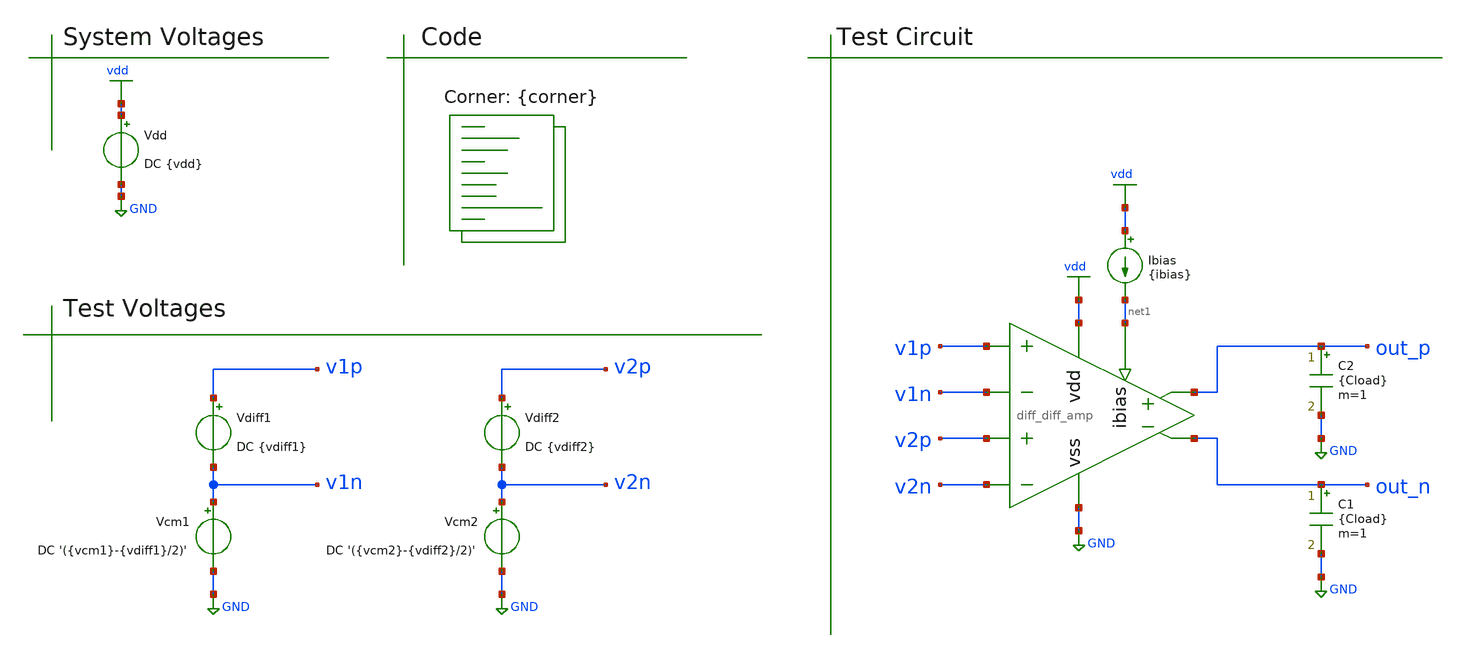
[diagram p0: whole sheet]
** sch_path: tb/tb_diffdiff_transfer.sch
**.subckt tb_diffdiff_transfer
Vdd vdd GND DC {vdd}
C1 out_n GND {Cload} m=1
Vdiff1 v1p v1n DC {vdiff1}
Vcm1 v1n GND DC '({vcm1}-{vdiff1}/2)'
C2 out_p GND {Cload} m=1
Vdiff2 v2p v2n DC {vdiff2}
Vcm2 v2n GND DC '({vcm2}-{vdiff2}/2)'
Ibias vdd net1 {ibias}
x1 v1p v1n v2p v2n out_p out_n net1 vdd GND diff_diff_amp
**** begin user architecture code


.option TEMP={temperature}
.option warn=1
.control
save out_p, out_n, i(vdd)
dc Vdiff1 -0.9 0.9 0.05
wrdata {output_file} V(out_p) V(out_n) I(vdd)
quit
.endc


.lib $::SKYWATER_MODELS/sky130.lib.spice {corner}
**** end user architecture code
**.ends

* expanding   symbol:  /home/moduhub/work/sky130_ak_ip__sigma_delta/sch/diff_diff_amp.sym # of
*+ pins=9
** sym_path: sch/diff_diff_amp.sym
** sch_path: sch/diff_diff_amp.sch
.subckt diff_diff_amp v1p v1n v2p v2n vo_p vo_n ibias vdd vss
*.ipin v1p
*.ipin v1n
*.ipin v2p
*.ipin v2n
*.ipin vss
*.ipin vdd
*.ipin ibias
*.opin vo_n
*.opin vo_p
XM1 net1 ibias vss vss sky130_fd_pr__nfet_01v8 L=0.5 W=10 nf=1 ad='int((nf+1)/2) * W/nf * 0.29' as='int((nf+2)/2) * W/nf * 0.29'
+ pd='2*int((nf+1)/2) * (W/nf + 0.29)' ps='2*int((nf+2)/2) * (W/nf + 0.29)' nrd='0.29 / W' nrs='0.29 / W'
+ sa=0 sb=0 sd=0 mult=1 m=1
XM2 net2 ibias vss vss sky130_fd_pr__nfet_01v8 L=0.5 W=10 nf=1 ad='int((nf+1)/2) * W/nf * 0.29' as='int((nf+2)/2) * W/nf * 0.29'
+ pd='2*int((nf+1)/2) * (W/nf + 0.29)' ps='2*int((nf+2)/2) * (W/nf + 0.29)' nrd='0.29 / W' nrs='0.29 / W'
+ sa=0 sb=0 sd=0 mult=1 m=1
XM3 ibias ibias vss vss sky130_fd_pr__nfet_01v8 L=0.5 W=1 nf=1 ad='int((nf+1)/2) * W/nf * 0.29' as='int((nf+2)/2) * W/nf * 0.29'
+ pd='2*int((nf+1)/2) * (W/nf + 0.29)' ps='2*int((nf+2)/2) * (W/nf + 0.29)' nrd='0.29 / W' nrs='0.29 / W'
+ sa=0 sb=0 sd=0 mult=1 m=1
XM4 vo_n v1p net1 vss sky130_fd_pr__nfet_01v8 L=1 W=4 nf=1 ad='int((nf+1)/2) * W/nf * 0.29' as='int((nf+2)/2) * W/nf * 0.29'
+ pd='2*int((nf+1)/2) * (W/nf + 0.29)' ps='2*int((nf+2)/2) * (W/nf + 0.29)' nrd='0.29 / W' nrs='0.29 / W'
+ sa=0 sb=0 sd=0 mult=1 m=1
XM5 vo_p v1n net1 vss sky130_fd_pr__nfet_01v8 L=1 W=4 nf=1 ad='int((nf+1)/2) * W/nf * 0.29' as='int((nf+2)/2) * W/nf * 0.29'
+ pd='2*int((nf+1)/2) * (W/nf + 0.29)' ps='2*int((nf+2)/2) * (W/nf + 0.29)' nrd='0.29 / W' nrs='0.29 / W'
+ sa=0 sb=0 sd=0 mult=1 m=1
XM6 vo_n v2p net2 vss sky130_fd_pr__nfet_01v8 L=1 W=4 nf=1 ad='int((nf+1)/2) * W/nf * 0.29' as='int((nf+2)/2) * W/nf * 0.29'
+ pd='2*int((nf+1)/2) * (W/nf + 0.29)' ps='2*int((nf+2)/2) * (W/nf + 0.29)' nrd='0.29 / W' nrs='0.29 / W'
+ sa=0 sb=0 sd=0 mult=1 m=1
XM7 vo_p v2n net2 vss sky130_fd_pr__nfet_01v8 L=1 W=4 nf=1 ad='int((nf+1)/2) * W/nf * 0.29' as='int((nf+2)/2) * W/nf * 0.29'
+ pd='2*int((nf+1)/2) * (W/nf + 0.29)' ps='2*int((nf+2)/2) * (W/nf + 0.29)' nrd='0.29 / W' nrs='0.29 / W'
+ sa=0 sb=0 sd=0 mult=1 m=1
XR1 vo_n vdd vdd sky130_fd_pr__res_xhigh_po_1p41 L=100 mult=1 m=1
XR2 vo_p vdd vdd sky130_fd_pr__res_xhigh_po_1p41 L=100 mult=1 m=1
.ends

.GLOBAL vdd
.GLOBAL GND
.end
